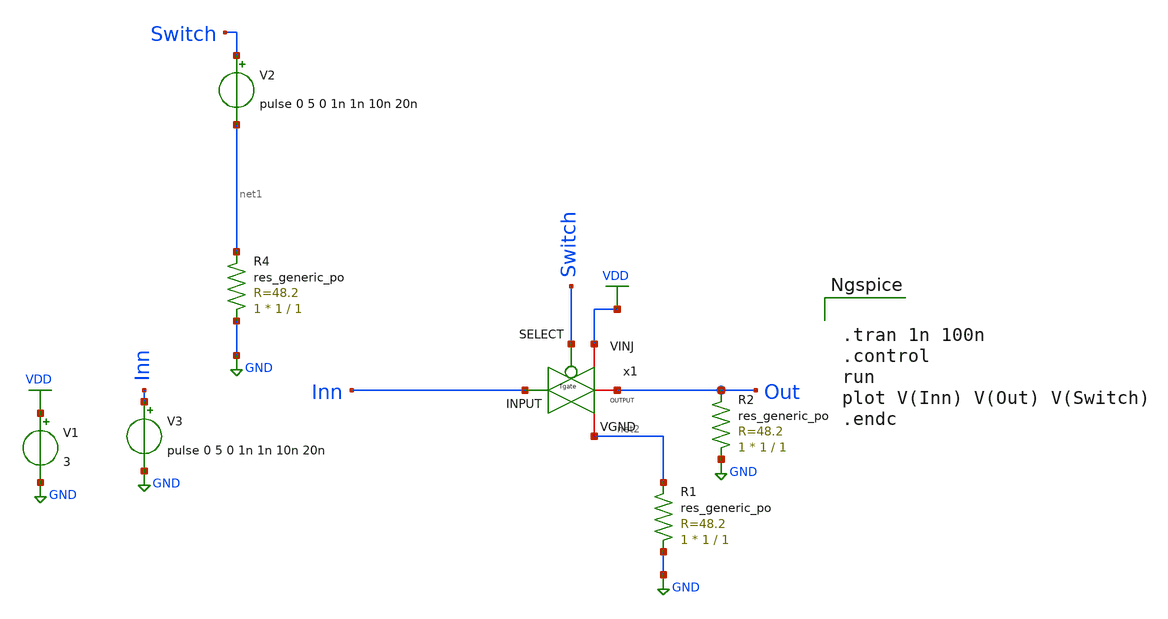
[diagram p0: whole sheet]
** sch_path: sky130_cells/Practice/Capacitor_Array/Schematic/TgateSmallSim.sch
**.subckt TgateSmallSim
x1 VDD Out Switch Inn net2 Tgate
V2 Switch net1 pulse 0 5 0 1n 1n 10n 20n
V3 Inn GND pulse 0 5 0 1n 1n 10n 20n
V1 VDD GND 3
XR4 GND net1 sky130_fd_pr__res_generic_po W=1 L=1 m=1
XR1 GND net2 sky130_fd_pr__res_generic_po W=1 L=1 m=1
XR2 GND Out sky130_fd_pr__res_generic_po W=1 L=1 m=1
**** begin user architecture code

** opencircuitdesign pdks install
.lib $::SKYWATER_MODELS/sky130.lib.spice tt




.tran 1n 100n
.control
run
plot V(Inn) V(Out) V(Switch)
.endc


**** end user architecture code
**.ends

* expanding   symbol:  sky130_cells/RDAC/Design/Tgate.sym # of pins=5
** sym_path: sky130_cells/RDAC/Design/Tgate.sym
** sch_path: sky130_cells/RDAC/Design/Tgate.sch
.subckt Tgate VINJ OUTPUT SELECT INPUT VGND
*.iopin VINJ
*.ipin SELECT
*.iopin INPUT
*.iopin OUTPUT
*.ipin VGND
XM5 net1 SELECT VGND VGND sky130_fd_pr__nfet_g5v0d10v5 L=0.5 W=0.42 nf=1 ad='int((1 + 1)/2) * 0.42 / 1 * 0.29'
+ as='int((1 + 2)/2) * 0.42 / 1 * 0.29' pd='2*int((1 + 1)/2) * (0.42 / 1 + 0.29)' ps='2*int((1 + 2)/2) * (0.42 / 1 + 0.29)'
+ nrd='0.29 / 0.42 ' nrs='0.29 / 0.42 ' sa=0 sb=0 sd=0 mult=1 m=1
XM1 net1 SELECT VINJ VINJ sky130_fd_pr__pfet_g5v0d10v5 L=0.5 W=0.42 nf=1 ad='int((1 + 1)/2) * 0.42 / 1 * 0.29'
+ as='int((1 + 2)/2) * 0.42 / 1 * 0.29' pd='2*int((1 + 1)/2) * (0.42 / 1 + 0.29)' ps='2*int((1 + 2)/2) * (0.42 / 1 + 0.29)'
+ nrd='0.29 / 0.42 ' nrs='0.29 / 0.42 ' sa=0 sb=0 sd=0 mult=1 m=1
XM2 INPUT net1 OUTPUT VINJ sky130_fd_pr__pfet_g5v0d10v5 L=0.5 W=0.42 nf=1 ad='int((1 + 1)/2) * 0.42 / 1 * 0.29'
+ as='int((1 + 2)/2) * 0.42 / 1 * 0.29' pd='2*int((1 + 1)/2) * (0.42 / 1 + 0.29)' ps='2*int((1 + 2)/2) * (0.42 / 1 + 0.29)'
+ nrd='0.29 / 0.42 ' nrs='0.29 / 0.42 ' sa=0 sb=0 sd=0 mult=1 m=1
XM3 OUTPUT SELECT INPUT VGND sky130_fd_pr__nfet_g5v0d10v5 L=0.5 W=0.42 nf=1 ad='int((1 + 1)/2) * 0.42 / 1 * 0.29'
+ as='int((1 + 2)/2) * 0.42 / 1 * 0.29' pd='2*int((1 + 1)/2) * (0.42 / 1 + 0.29)' ps='2*int((1 + 2)/2) * (0.42 / 1 + 0.29)'
+ nrd='0.29 / 0.42 ' nrs='0.29 / 0.42 ' sa=0 sb=0 sd=0 mult=1 m=1
.ends

.GLOBAL GND
.GLOBAL VDD
.end
